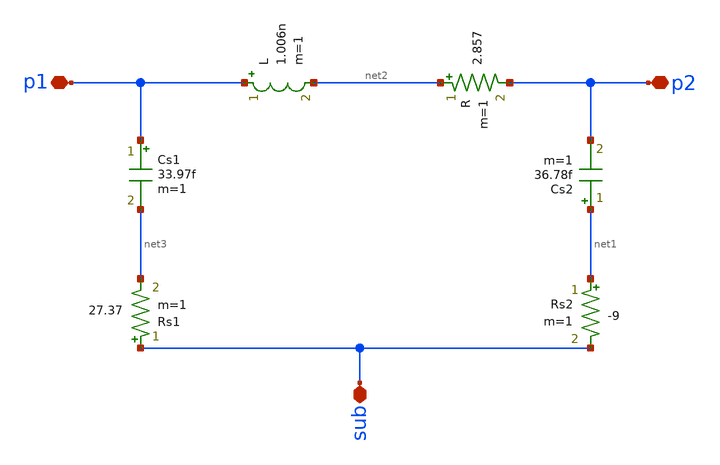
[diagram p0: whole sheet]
** sch_path: MICRO/inductor.sch
**.subckt inductor p1 p2 sub
*.iopin p1
*.iopin p2
*.iopin sub
L p1 net2 1.006n m=1
R net2 p2 2.857 m=1
Cs1 p1 net3 33.97f m=1
Cs2 net1 p2 36.78f m=1
Rs1 sub net3 27.37 m=1
Rs2 net1 sub -9 m=1
**.ends
.end
